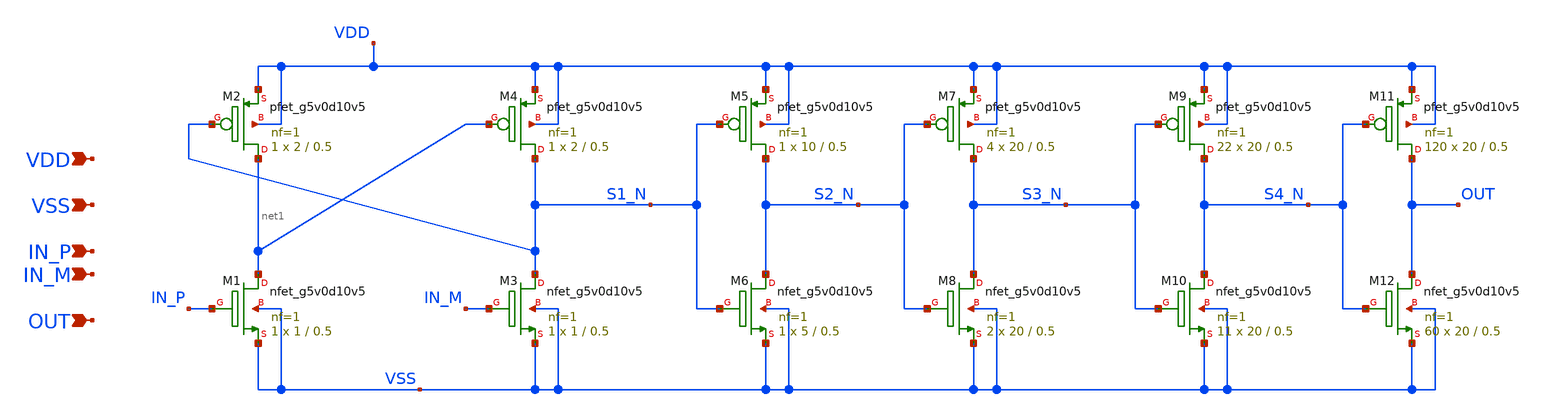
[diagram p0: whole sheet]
** sch_path: design/power-stage/gate_drive.sch
**.subckt gate_drive OUT VSS IN_P IN_M VDD
*.ipin OUT
*.ipin VSS
*.ipin IN_P
*.ipin IN_M
*.ipin VDD
XM1 net1 IN_P VSS VSS sky130_fd_pr__nfet_g5v0d10v5 L=0.5 W=1 nf=1 ad='int((nf+1)/2) * W/nf * 0.29' as='int((nf+2)/2) * W/nf * 0.29'
+ pd='2*int((nf+1)/2) * (W/nf + 0.29)' ps='2*int((nf+2)/2) * (W/nf + 0.29)' nrd='0.29 / W' nrs='0.29 / W'
+ sa=0 sb=0 sd=0 mult=1 m=1
XM2 net1 S1_N VDD VDD sky130_fd_pr__pfet_g5v0d10v5 L=0.5 W=2 nf=1 ad='int((nf+1)/2) * W/nf * 0.29' as='int((nf+2)/2) * W/nf * 0.29'
+ pd='2*int((nf+1)/2) * (W/nf + 0.29)' ps='2*int((nf+2)/2) * (W/nf + 0.29)' nrd='0.29 / W' nrs='0.29 / W'
+ sa=0 sb=0 sd=0 mult=1 m=1
XM3 S1_N IN_M VSS VSS sky130_fd_pr__nfet_g5v0d10v5 L=0.5 W=1 nf=1 ad='int((nf+1)/2) * W/nf * 0.29' as='int((nf+2)/2) * W/nf * 0.29'
+ pd='2*int((nf+1)/2) * (W/nf + 0.29)' ps='2*int((nf+2)/2) * (W/nf + 0.29)' nrd='0.29 / W' nrs='0.29 / W'
+ sa=0 sb=0 sd=0 mult=1 m=1
XM4 S1_N net1 VDD VDD sky130_fd_pr__pfet_g5v0d10v5 L=0.5 W=2 nf=1 ad='int((nf+1)/2) * W/nf * 0.29' as='int((nf+2)/2) * W/nf * 0.29'
+ pd='2*int((nf+1)/2) * (W/nf + 0.29)' ps='2*int((nf+2)/2) * (W/nf + 0.29)' nrd='0.29 / W' nrs='0.29 / W'
+ sa=0 sb=0 sd=0 mult=1 m=1
XM5 S2_N S1_N VDD VDD sky130_fd_pr__pfet_g5v0d10v5 L=0.5 W=10 nf=1 ad='int((nf+1)/2) * W/nf * 0.29' as='int((nf+2)/2) * W/nf * 0.29'
+ pd='2*int((nf+1)/2) * (W/nf + 0.29)' ps='2*int((nf+2)/2) * (W/nf + 0.29)' nrd='0.29 / W' nrs='0.29 / W'
+ sa=0 sb=0 sd=0 mult=1 m=1
XM6 S2_N S1_N VSS VSS sky130_fd_pr__nfet_g5v0d10v5 L=0.5 W=5 nf=1 ad='int((nf+1)/2) * W/nf * 0.29' as='int((nf+2)/2) * W/nf * 0.29'
+ pd='2*int((nf+1)/2) * (W/nf + 0.29)' ps='2*int((nf+2)/2) * (W/nf + 0.29)' nrd='0.29 / W' nrs='0.29 / W'
+ sa=0 sb=0 sd=0 mult=1 m=1
XM7 S3_N S2_N VDD VDD sky130_fd_pr__pfet_g5v0d10v5 L=0.5 W=20 nf=1 ad='int((nf+1)/2) * W/nf * 0.29' as='int((nf+2)/2) * W/nf * 0.29'
+ pd='2*int((nf+1)/2) * (W/nf + 0.29)' ps='2*int((nf+2)/2) * (W/nf + 0.29)' nrd='0.29 / W' nrs='0.29 / W'
+ sa=0 sb=0 sd=0 mult=4 m=4
XM8 S3_N S2_N VSS VSS sky130_fd_pr__nfet_g5v0d10v5 L=0.5 W=20 nf=1 ad='int((nf+1)/2) * W/nf * 0.29' as='int((nf+2)/2) * W/nf * 0.29'
+ pd='2*int((nf+1)/2) * (W/nf + 0.29)' ps='2*int((nf+2)/2) * (W/nf + 0.29)' nrd='0.29 / W' nrs='0.29 / W'
+ sa=0 sb=0 sd=0 mult=2 m=2
XM9 S4_N S3_N VDD VDD sky130_fd_pr__pfet_g5v0d10v5 L=0.5 W=20 nf=1 ad='int((nf+1)/2) * W/nf * 0.29' as='int((nf+2)/2) * W/nf * 0.29'
+ pd='2*int((nf+1)/2) * (W/nf + 0.29)' ps='2*int((nf+2)/2) * (W/nf + 0.29)' nrd='0.29 / W' nrs='0.29 / W'
+ sa=0 sb=0 sd=0 mult=22 m=22
XM10 S4_N S3_N VSS VSS sky130_fd_pr__nfet_g5v0d10v5 L=0.5 W=20 nf=1 ad='int((nf+1)/2) * W/nf * 0.29'
+ as='int((nf+2)/2) * W/nf * 0.29' pd='2*int((nf+1)/2) * (W/nf + 0.29)' ps='2*int((nf+2)/2) * (W/nf + 0.29)'
+ nrd='0.29 / W' nrs='0.29 / W' sa=0 sb=0 sd=0 mult=11 m=11
XM11 OUT S4_N VDD VDD sky130_fd_pr__pfet_g5v0d10v5 L=0.5 W=20 nf=1 ad='int((nf+1)/2) * W/nf * 0.29' as='int((nf+2)/2) * W/nf * 0.29'
+ pd='2*int((nf+1)/2) * (W/nf + 0.29)' ps='2*int((nf+2)/2) * (W/nf + 0.29)' nrd='0.29 / W' nrs='0.29 / W'
+ sa=0 sb=0 sd=0 mult=120 m=120
XM12 OUT S4_N VSS VSS sky130_fd_pr__nfet_g5v0d10v5 L=0.5 W=20 nf=1 ad='int((nf+1)/2) * W/nf * 0.29' as='int((nf+2)/2) * W/nf * 0.29'
+ pd='2*int((nf+1)/2) * (W/nf + 0.29)' ps='2*int((nf+2)/2) * (W/nf + 0.29)' nrd='0.29 / W' nrs='0.29 / W'
+ sa=0 sb=0 sd=0 mult=60 m=60
**.ends
.end
